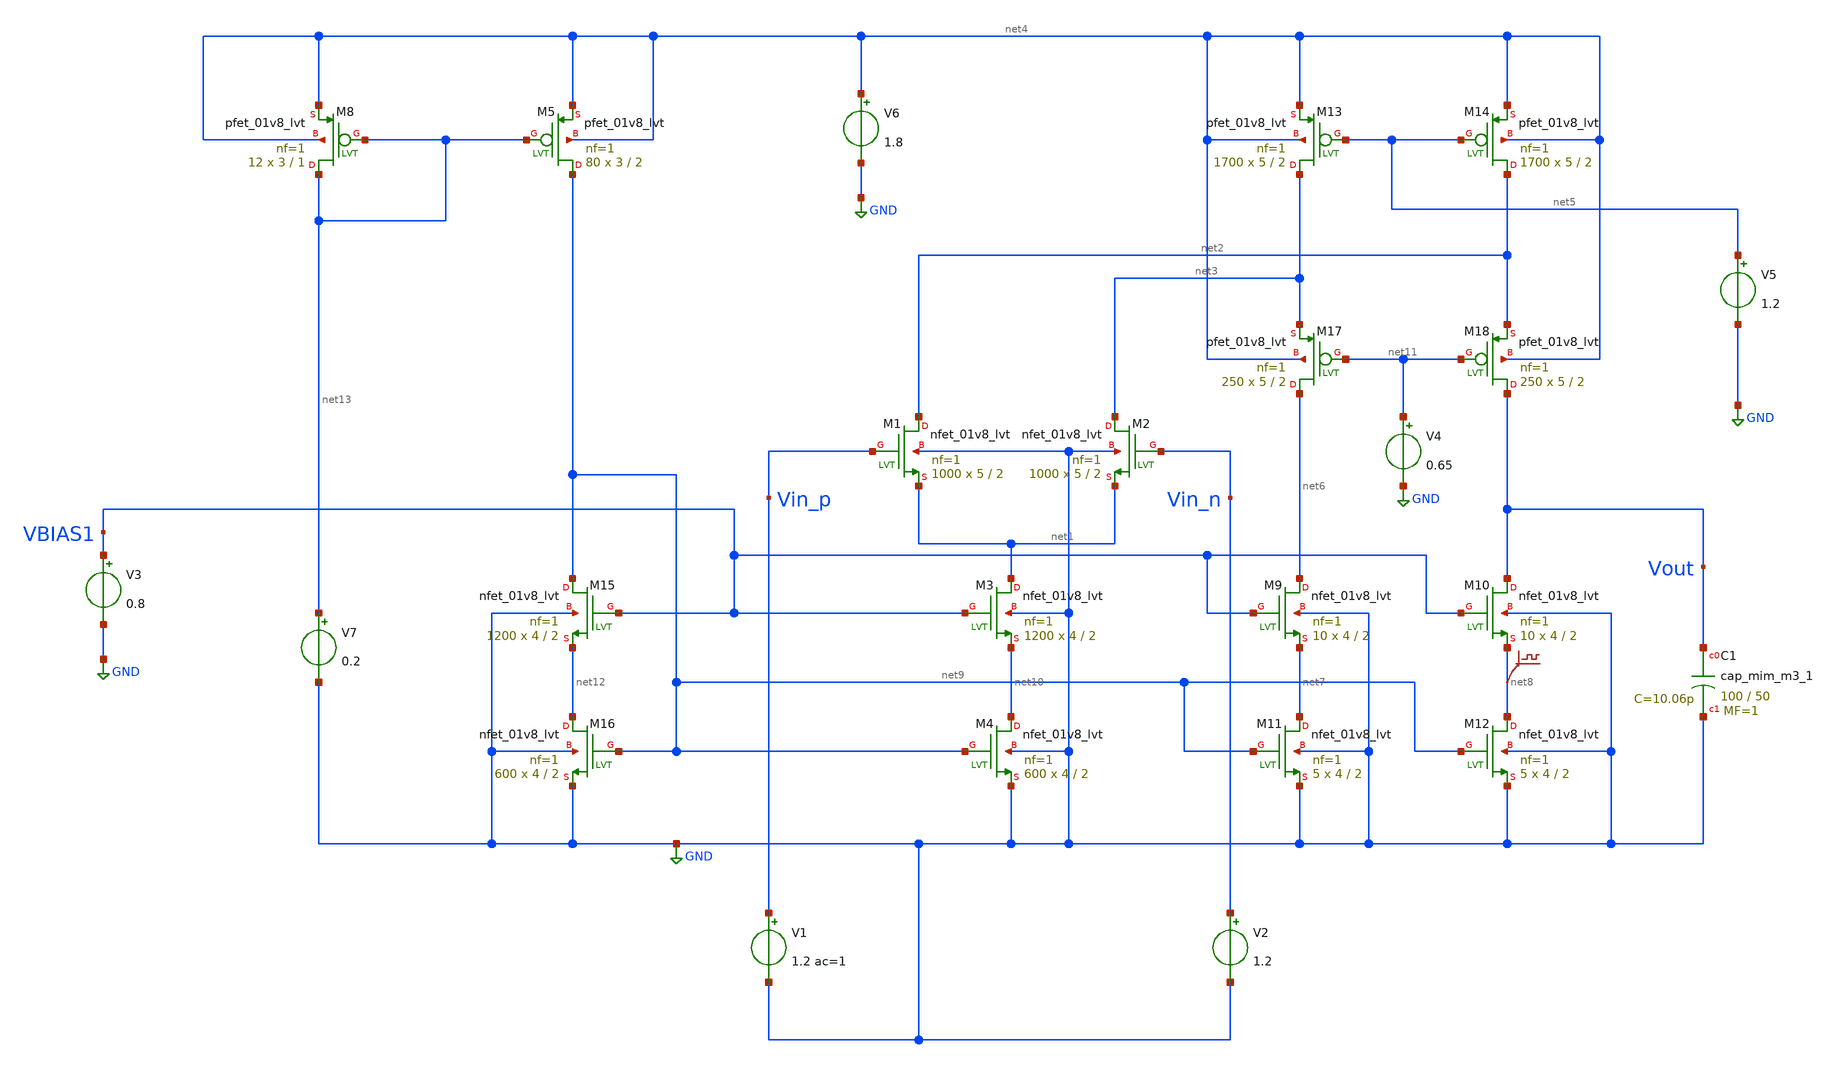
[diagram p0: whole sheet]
** sch_path: xschem/OTA/OTA-2.0.sch
**.subckt OTA-2.0
XM1 net2 Vin_p net1 GND sky130_fd_pr__nfet_01v8_lvt L=2 W=5 nf=1 ad='int((nf+1)/2) * W/nf * 0.29' as='int((nf+2)/2) * W/nf * 0.29'
+ pd='2*int((nf+1)/2) * (W/nf + 0.29)' ps='2*int((nf+2)/2) * (W/nf + 0.29)' nrd='0.29 / W' nrs='0.29 / W'
+ sa=0 sb=0 sd=0 mult=1000 m=1000
XM2 net3 Vin_n net1 GND sky130_fd_pr__nfet_01v8_lvt L=2 W=5 nf=1 ad='int((nf+1)/2) * W/nf * 0.29' as='int((nf+2)/2) * W/nf * 0.29'
+ pd='2*int((nf+1)/2) * (W/nf + 0.29)' ps='2*int((nf+2)/2) * (W/nf + 0.29)' nrd='0.29 / W' nrs='0.29 / W'
+ sa=0 sb=0 sd=0 mult=1000 m=1000
XM3 net1 VBIAS1 net10 GND sky130_fd_pr__nfet_01v8_lvt L=2 W=4 nf=1 ad='int((nf+1)/2) * W/nf * 0.29' as='int((nf+2)/2) * W/nf * 0.29'
+ pd='2*int((nf+1)/2) * (W/nf + 0.29)' ps='2*int((nf+2)/2) * (W/nf + 0.29)' nrd='0.29 / W' nrs='0.29 / W'
+ sa=0 sb=0 sd=0 mult=1200 m=1200
XM4 net10 net9 GND GND sky130_fd_pr__nfet_01v8_lvt L=2 W=4 nf=1 ad='int((nf+1)/2) * W/nf * 0.29' as='int((nf+2)/2) * W/nf * 0.29'
+ pd='2*int((nf+1)/2) * (W/nf + 0.29)' ps='2*int((nf+2)/2) * (W/nf + 0.29)' nrd='0.29 / W' nrs='0.29 / W'
+ sa=0 sb=0 sd=0 mult=600 m=600
XM9 net6 VBIAS1 net7 GND sky130_fd_pr__nfet_01v8_lvt L=2 W=4 nf=1 ad='int((nf+1)/2) * W/nf * 0.29' as='int((nf+2)/2) * W/nf * 0.29'
+ pd='2*int((nf+1)/2) * (W/nf + 0.29)' ps='2*int((nf+2)/2) * (W/nf + 0.29)' nrd='0.29 / W' nrs='0.29 / W'
+ sa=0 sb=0 sd=0 mult=10 m=10
XM10 Vout VBIAS1 net8 GND sky130_fd_pr__nfet_01v8_lvt L=2 W=4 nf=1 ad='int((nf+1)/2) * W/nf * 0.29' as='int((nf+2)/2) * W/nf * 0.29'
+ pd='2*int((nf+1)/2) * (W/nf + 0.29)' ps='2*int((nf+2)/2) * (W/nf + 0.29)' nrd='0.29 / W' nrs='0.29 / W'
+ sa=0 sb=0 sd=0 mult=10 m=10
XM11 net7 net9 GND GND sky130_fd_pr__nfet_01v8_lvt L=2 W=4 nf=1 ad='int((nf+1)/2) * W/nf * 0.29' as='int((nf+2)/2) * W/nf * 0.29'
+ pd='2*int((nf+1)/2) * (W/nf + 0.29)' ps='2*int((nf+2)/2) * (W/nf + 0.29)' nrd='0.29 / W' nrs='0.29 / W'
+ sa=0 sb=0 sd=0 mult=5 m=5
XM12 net8 net9 GND GND sky130_fd_pr__nfet_01v8_lvt L=2 W=4 nf=1 ad='int((nf+1)/2) * W/nf * 0.29' as='int((nf+2)/2) * W/nf * 0.29'
+ pd='2*int((nf+1)/2) * (W/nf + 0.29)' ps='2*int((nf+2)/2) * (W/nf + 0.29)' nrd='0.29 / W' nrs='0.29 / W'
+ sa=0 sb=0 sd=0 mult=5 m=5
V1 Vin_p GND 1.2 ac=1
V2 Vin_n GND 1.2
XM15 net9 VBIAS1 net12 GND sky130_fd_pr__nfet_01v8_lvt L=2 W=4 nf=1 ad='int((nf+1)/2) * W/nf * 0.29'
+ as='int((nf+2)/2) * W/nf * 0.29' pd='2*int((nf+1)/2) * (W/nf + 0.29)' ps='2*int((nf+2)/2) * (W/nf + 0.29)'
+ nrd='0.29 / W' nrs='0.29 / W' sa=0 sb=0 sd=0 mult=1200 m=1200
XM16 net12 net9 GND GND sky130_fd_pr__nfet_01v8_lvt L=2 W=4 nf=1 ad='int((nf+1)/2) * W/nf * 0.29' as='int((nf+2)/2) * W/nf * 0.29'
+ pd='2*int((nf+1)/2) * (W/nf + 0.29)' ps='2*int((nf+2)/2) * (W/nf + 0.29)' nrd='0.29 / W' nrs='0.29 / W'
+ sa=0 sb=0 sd=0 mult=600 m=600
V3 VBIAS1 GND 0.8
.save v(net8)
V6 net4 GND 1.8
XM8 net13 net13 net4 net4 sky130_fd_pr__pfet_01v8_lvt L=1 W=3 nf=1 ad='int((nf+1)/2) * W/nf * 0.29' as='int((nf+2)/2) * W/nf * 0.29'
+ pd='2*int((nf+1)/2) * (W/nf + 0.29)' ps='2*int((nf+2)/2) * (W/nf + 0.29)' nrd='0.29 / W' nrs='0.29 / W'
+ sa=0 sb=0 sd=0 mult=12 m=12
XM5 net9 net13 net4 net4 sky130_fd_pr__pfet_01v8_lvt L=2 W=3 nf=1 ad='int((nf+1)/2) * W/nf * 0.29' as='int((nf+2)/2) * W/nf * 0.29'
+ pd='2*int((nf+1)/2) * (W/nf + 0.29)' ps='2*int((nf+2)/2) * (W/nf + 0.29)' nrd='0.29 / W' nrs='0.29 / W'
+ sa=0 sb=0 sd=0 mult=80 m=80
XM13 net3 net5 net4 net4 sky130_fd_pr__pfet_01v8_lvt L=2 W=5 nf=1 ad='int((nf+1)/2) * W/nf * 0.29' as='int((nf+2)/2) * W/nf * 0.29'
+ pd='2*int((nf+1)/2) * (W/nf + 0.29)' ps='2*int((nf+2)/2) * (W/nf + 0.29)' nrd='0.29 / W' nrs='0.29 / W'
+ sa=0 sb=0 sd=0 mult=1700 m=1700
XM14 net2 net5 net4 net4 sky130_fd_pr__pfet_01v8_lvt L=2 W=5 nf=1 ad='int((nf+1)/2) * W/nf * 0.29' as='int((nf+2)/2) * W/nf * 0.29'
+ pd='2*int((nf+1)/2) * (W/nf + 0.29)' ps='2*int((nf+2)/2) * (W/nf + 0.29)' nrd='0.29 / W' nrs='0.29 / W'
+ sa=0 sb=0 sd=0 mult=1700 m=1700
XM17 net6 net11 net3 net4 sky130_fd_pr__pfet_01v8_lvt L=2 W=5 nf=1 ad='int((nf+1)/2) * W/nf * 0.29' as='int((nf+2)/2) * W/nf * 0.29'
+ pd='2*int((nf+1)/2) * (W/nf + 0.29)' ps='2*int((nf+2)/2) * (W/nf + 0.29)' nrd='0.29 / W' nrs='0.29 / W'
+ sa=0 sb=0 sd=0 mult=250 m=250
XM18 Vout net11 net2 net4 sky130_fd_pr__pfet_01v8_lvt L=2 W=5 nf=1 ad='int((nf+1)/2) * W/nf * 0.29' as='int((nf+2)/2) * W/nf * 0.29'
+ pd='2*int((nf+1)/2) * (W/nf + 0.29)' ps='2*int((nf+2)/2) * (W/nf + 0.29)' nrd='0.29 / W' nrs='0.29 / W'
+ sa=0 sb=0 sd=0 mult=250 m=250
XC1 Vout GND sky130_fd_pr__cap_mim_m3_1 W=100 L=50 MF=1 m=1
V4 net11 GND 0.65
V5 net5 GND 1.2
V7 net13 GND 0.2
**** begin user architecture code

** opencircuitdesign pdks install
.lib $::SKYWATER_MODELS/sky130.lib.spice tt




.option temp=27

*.op
*.ac dec 10 1 1G
*.tran 0.001 0.2u 10n

.control
save all
run
ac dec 10 1 1G
*tran 1u 10u
display
*ac dec 10 1 1G
let phase = 180/PI*vp(Vout)

plot vdb(Vout) phase
*plot Vin_p Vout
.endc

.save all



**** end user architecture code
**.ends
.GLOBAL GND
.end
